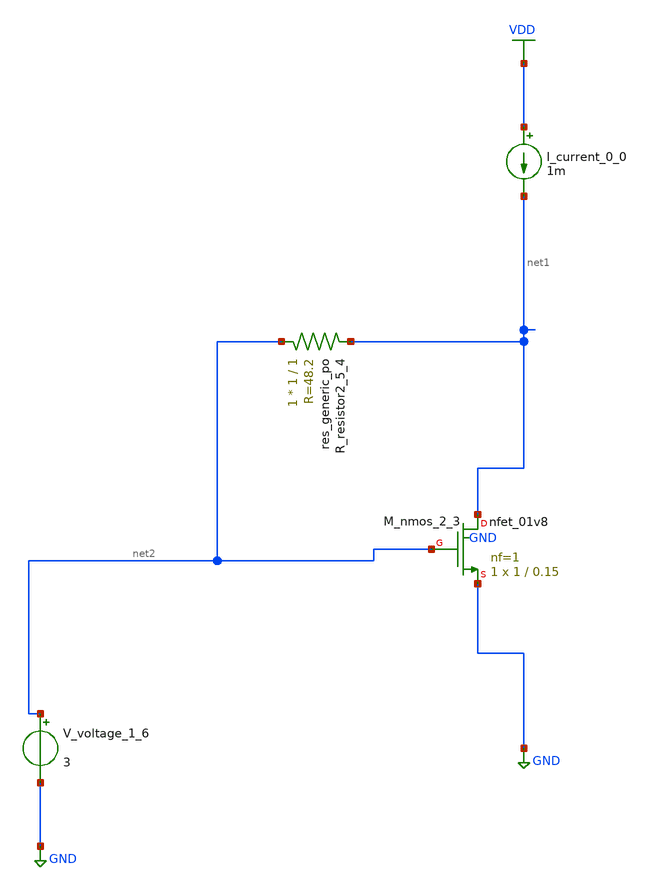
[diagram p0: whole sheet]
** sch_path: schematics/AMSNet/33.sch
**.subckt 33
I_current_0_0 VDD net1 1m
XM_nmos_2_3 net1 net2 GND GND sky130_fd_pr__nfet_01v8 L=0.15 W=1 nf=1 ad='int((1 + 1)/2) * 1 / 1 * 0.29'
+ as='int((1 + 2)/2) * 1 / 1 * 0.29' pd='2*int((1 + 1)/2) * (1 / 1 + 0.29)' ps='2*int((1 + 2)/2) * (1 / 1 + 0.29)'
+ nrd='0.29 / 1 ' nrs='0.29 / 1 ' sa=0 sb=0 sd=0 mult=1 m=1
XR_resistor2_5_4 net2 net1 sky130_fd_pr__res_generic_po W=1 L=1 m=1
V_voltage_1_6 net2 GND 3
**.ends
.GLOBAL GND
.GLOBAL VDD
.end
